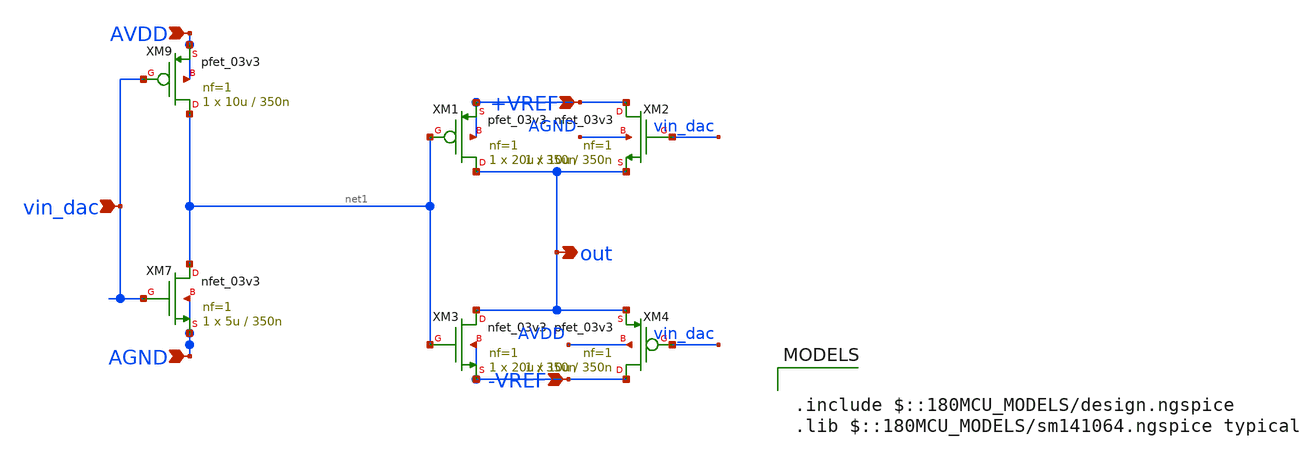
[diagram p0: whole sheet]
** sch_path: 1-bitDAC.sch
**.subckt 1-bitDAC vin_dac out AVDD AGND +VREF -VREF
*.ipin vin_dac
*.opin out
*.ipin AVDD
*.ipin AGND
*.ipin +VREF
*.ipin -VREF
XM7 net1 vin_dac AGND AGND nfet_03v3 L=350n W=5u nf=1 ad='int((nf+1)/2) * W/nf * 0.18u' as='int((nf+2)/2) * W/nf * 0.18u'
+ pd='2*int((nf+1)/2) * (W/nf + 0.18u)' ps='2*int((nf+2)/2) * (W/nf + 0.18u)' nrd='0.18u / W' nrs='0.18u / W'
+ sa=0 sb=0 sd=0 m=1
XM9 net1 vin_dac AVDD AVDD pfet_03v3 L=350n W=10u nf=1 ad='int((nf+1)/2) * W/nf * 0.18u' as='int((nf+2)/2) * W/nf * 0.18u'
+ pd='2*int((nf+1)/2) * (W/nf + 0.18u)' ps='2*int((nf+2)/2) * (W/nf + 0.18u)' nrd='0.18u / W' nrs='0.18u / W'
+ sa=0 sb=0 sd=0 m=1
XM1 out net1 +VREF +VREF pfet_03v3 L=350n W=20u nf=1 ad='int((nf+1)/2) * W/nf * 0.18u' as='int((nf+2)/2) * W/nf * 0.18u'
+ pd='2*int((nf+1)/2) * (W/nf + 0.18u)' ps='2*int((nf+2)/2) * (W/nf + 0.18u)' nrd='0.18u / W' nrs='0.18u / W'
+ sa=0 sb=0 sd=0 m=1
XM2 +VREF vin_dac out AGND nfet_03v3 L=350n W=10u nf=1 ad='int((nf+1)/2) * W/nf * 0.18u' as='int((nf+2)/2) * W/nf * 0.18u'
+ pd='2*int((nf+1)/2) * (W/nf + 0.18u)' ps='2*int((nf+2)/2) * (W/nf + 0.18u)' nrd='0.18u / W' nrs='0.18u / W'
+ sa=0 sb=0 sd=0 m=1
XM3 out net1 -VREF -VREF nfet_03v3 L=350n W=20u nf=1 ad='int((nf+1)/2) * W/nf * 0.18u' as='int((nf+2)/2) * W/nf * 0.18u'
+ pd='2*int((nf+1)/2) * (W/nf + 0.18u)' ps='2*int((nf+2)/2) * (W/nf + 0.18u)' nrd='0.18u / W' nrs='0.18u / W'
+ sa=0 sb=0 sd=0 m=1
XM4 -VREF vin_dac out AVDD pfet_03v3 L=350n W=10u nf=1 ad='int((nf+1)/2) * W/nf * 0.18u' as='int((nf+2)/2) * W/nf * 0.18u'
+ pd='2*int((nf+1)/2) * (W/nf + 0.18u)' ps='2*int((nf+2)/2) * (W/nf + 0.18u)' nrd='0.18u / W' nrs='0.18u / W'
+ sa=0 sb=0 sd=0 m=1
**** begin user architecture code

.include $::180MCU_MODELS/design.ngspice
.lib $::180MCU_MODELS/sm141064.ngspice typical

**** end user architecture code
**.ends
.end
